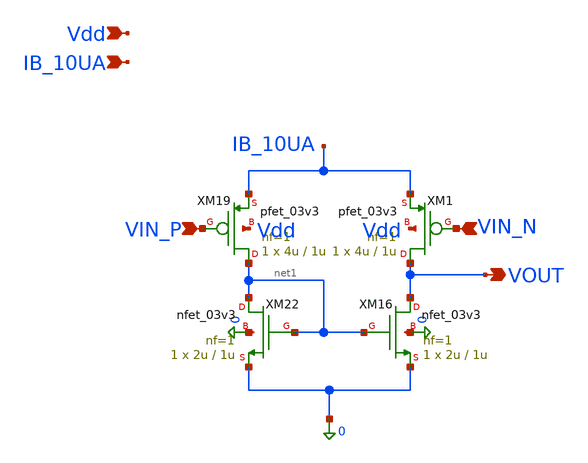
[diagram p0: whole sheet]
** sch_path: blocks/dac/common/ota5t.sch
**.subckt ota5t VIN_P VIN_N VOUT Vdd IB_10UA
*.ipin VIN_P
*.ipin VIN_N
*.opin VOUT
*.ipin Vdd
*.ipin IB_10UA
XM16 VOUT net1 0 0 nfet_03v3 L=1u W=2u nf=1 ad='int((nf+1)/2) * W/nf * 0.18u' as='int((nf+2)/2) * W/nf * 0.18u'
+ pd='2*int((nf+1)/2) * (W/nf + 0.18u)' ps='2*int((nf+2)/2) * (W/nf + 0.18u)' nrd='0.18u / W' nrs='0.18u / W'
+ sa=0 sb=0 sd=0 m=1
XM1 VOUT VIN_N IB_10UA Vdd pfet_03v3 L=1u W=4u nf=1 ad='int((nf+1)/2) * W/nf * 0.18u' as='int((nf+2)/2) * W/nf * 0.18u'
+ pd='2*int((nf+1)/2) * (W/nf + 0.18u)' ps='2*int((nf+2)/2) * (W/nf + 0.18u)' nrd='0.18u / W' nrs='0.18u / W'
+ sa=0 sb=0 sd=0 m=1
XM19 net1 VIN_P IB_10UA Vdd pfet_03v3 L=1u W=4u nf=1 ad='int((nf+1)/2) * W/nf * 0.18u' as='int((nf+2)/2) * W/nf * 0.18u'
+ pd='2*int((nf+1)/2) * (W/nf + 0.18u)' ps='2*int((nf+2)/2) * (W/nf + 0.18u)' nrd='0.18u / W' nrs='0.18u / W'
+ sa=0 sb=0 sd=0 m=1
XM22 net1 net1 0 0 nfet_03v3 L=1u W=2u nf=1 ad='int((nf+1)/2) * W/nf * 0.18u' as='int((nf+2)/2) * W/nf * 0.18u'
+ pd='2*int((nf+1)/2) * (W/nf + 0.18u)' ps='2*int((nf+2)/2) * (W/nf + 0.18u)' nrd='0.18u / W' nrs='0.18u / W'
+ sa=0 sb=0 sd=0 m=1
**.ends
.end
